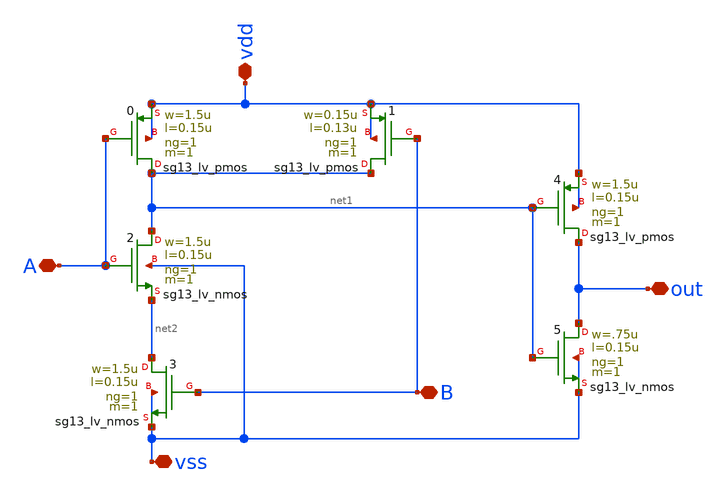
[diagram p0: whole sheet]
** sch_path: design/blocks/and2/schematic/and2.sch
**.subckt and2 A B vss vdd out
*.iopin A
*.iopin B
*.iopin vss
*.iopin vdd
*.iopin out
X2 net1 A net2 vss sg13_lv_nmos w=1.5u l=0.15u ng=1 m=1 mm_ok=1
X0 net1 A vdd vdd sg13_lv_pmos w=1.5u l=0.15u ng=1 m=1 mm_ok=1
X3 net2 B vss vss sg13_lv_nmos w=1.5u l=0.15u ng=1 m=1 mm_ok=1
X1 net1 B vdd vdd sg13_lv_pmos w=0.15u l=0.13u ng=1 m=1 mm_ok=1
X4 out net1 vdd vdd sg13_lv_pmos w=1.5u l=0.15u ng=1 m=1 mm_ok=1
X5 out net1 vss vss sg13_lv_nmos w=.75u l=0.15u ng=1 m=1 mm_ok=1
**.ends
.end
